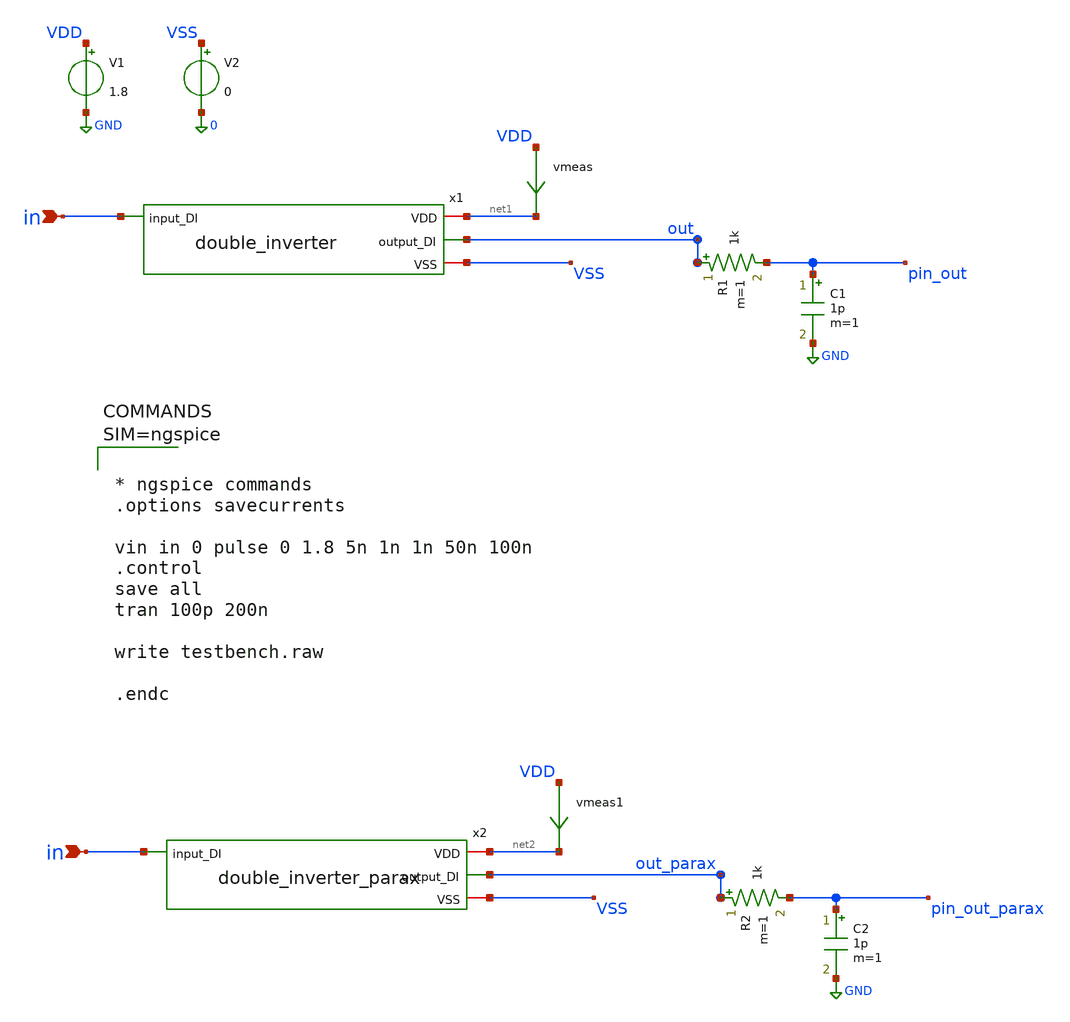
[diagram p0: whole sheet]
** sch_path: xschem/testbench.sch
**.subckt testbench in in
*.ipin in
*.ipin in
x1 net1 in out VSS double_inverter
V1 VDD GND 1.8
V2 VSS 0 0
R1 out pin_out 1k m=1
C1 pin_out GND 1p m=1
vmeas VDD net1 0
.save i(vmeas)
x2 net2 in out_parax VSS double_inverter_parax
R2 out_parax pin_out_parax 1k m=1
C2 pin_out_parax GND 1p m=1
vmeas1 VDD net2 0
.save i(vmeas1)
**** begin user architecture code

** opencircuitdesign pdks install
.lib $::SKYWATER_MODELS/sky130.lib.spice tt




* ngspice commands
.options savecurrents

vin in 0 pulse 0 1.8 5n 1n 1n 50n 100n
.control
save all
tran 100p 200n

write testbench.raw

.endc



**** end user architecture code
**.ends

* expanding   symbol:  double_inverter.sym # of pins=4
** sym_path: xschem/double_inverter.sym
** sch_path: xschem/double_inverter.sch
.subckt double_inverter VDD input_DI output_DI VSS
*.iopin VDD
*.iopin VSS
*.ipin input_DI
*.opin output_DI
XM1 inverted input_DI VSS VSS sky130_fd_pr__nfet_01v8 L=0.15 W=1 nf=1 ad='int((1 + 1)/2) * 1 / 1 * 0.29'
+ as='int((1 + 2)/2) * 1 / 1 * 0.29' pd='2*int((1 + 1)/2) * (1 / 1 + 0.29)' ps='2*int((1 + 2)/2) * (1 / 1 + 0.29)'
+ nrd='0.29 / 1 ' nrs='0.29 / 1 ' sa=0 sb=0 sd=0 mult=1 m=1
XM2 inverted input_DI VDD VDD sky130_fd_pr__pfet_01v8 L=0.15 W=1 nf=1 ad='int((1 + 1)/2) * 1 / 1 * 0.29'
+ as='int((1 + 2)/2) * 1 / 1 * 0.29' pd='2*int((1 + 1)/2) * (1 / 1 + 0.29)' ps='2*int((1 + 2)/2) * (1 / 1 + 0.29)'
+ nrd='0.29 / 1 ' nrs='0.29 / 1 ' sa=0 sb=0 sd=0 mult=1 m=1
XM3 output_DI inverted VSS VSS sky130_fd_pr__nfet_01v8 L=0.15 W=20 nf=20 ad='int((20 + 1)/2) * 20 / 20 * 0.29'
+ as='int((20 + 2)/2) * 20 / 20 * 0.29' pd='2*int((20 + 1)/2) * (20 / 20 + 0.29)' ps='2*int((20 + 2)/2) * (20 / 20 + 0.29)'
+ nrd='0.29 / 20 ' nrs='0.29 / 20 ' sa=0 sb=0 sd=0 mult=1 m=1
XM4 output_DI inverted VDD VDD sky130_fd_pr__pfet_01v8 L=0.15 W=20 nf=20 ad='int((20 + 1)/2) * 20 / 20 * 0.29'
+ as='int((20 + 2)/2) * 20 / 20 * 0.29' pd='2*int((20 + 1)/2) * (20 / 20 + 0.29)' ps='2*int((20 + 2)/2) * (20 / 20 + 0.29)'
+ nrd='0.29 / 20 ' nrs='0.29 / 20 ' sa=0 sb=0 sd=0 mult=1 m=1
.ends


* expanding   symbol:  double_inverter_parax.sym # of pins=4
** sym_path: xschem/double_inverter.sym
.include [file normalize ../mag/double_inverter.sim.spice]
.GLOBAL GND
.end
